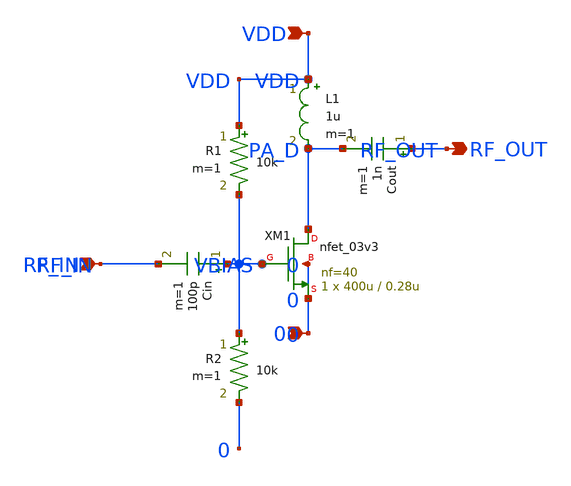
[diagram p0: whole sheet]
** sch_path: modules/PandaChip/designs/rf_trans/pa.sch
**.subckt pa VDD RF_IN RF_OUT 0
*.ipin VDD
*.ipin RF_IN
*.opin RF_OUT
*.ipin 0
XM1 PA_D VBIAS 0 0 nfet_03v3 L=0.28u W=400u nf=40 ad='int((nf+1)/2) * W/nf * 0.18u' as='int((nf+2)/2) * W/nf * 0.18u'
+ pd='2*int((nf+1)/2) * (W/nf + 0.18u)' ps='2*int((nf+2)/2) * (W/nf + 0.18u)' nrd='0.18u / W' nrs='0.18u / W'
+ sa=0 sb=0 sd=0 m=1
L1 VDD PA_D 1u m=1
Cout RF_OUT PA_D 1n m=1
Cin VBIAS RF_IN 100p m=1
R1 VDD VBIAS 10k m=1
R2 VBIAS 0 10k m=1
**.ends
.end
